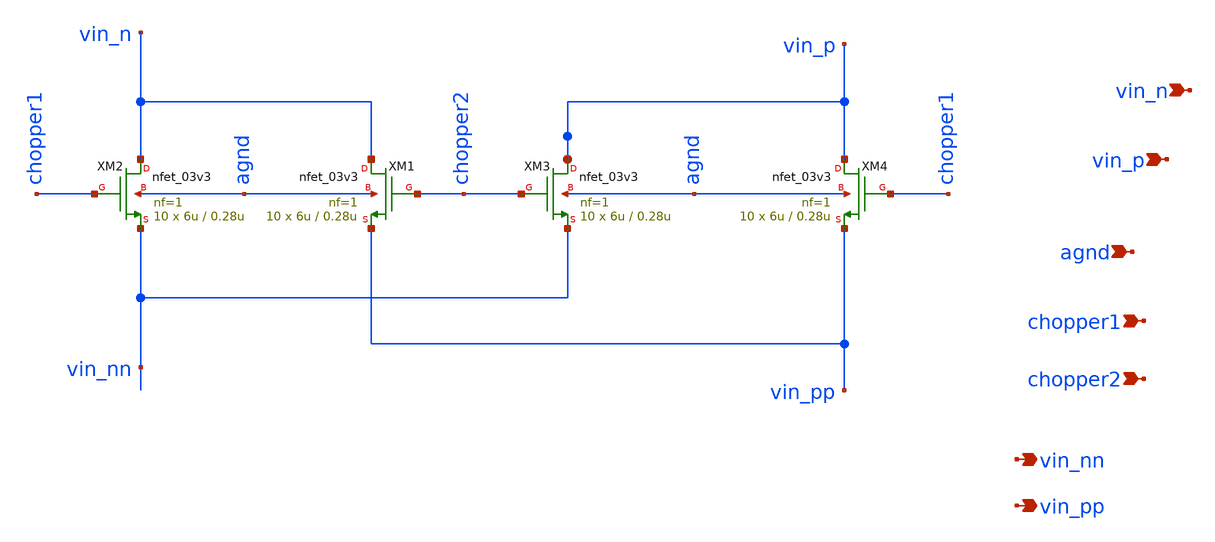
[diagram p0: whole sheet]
** sch_path: ABC123_SDC/design_data/xschem/CHOPPER/chopper.sch
**.subckt chopper vin_n vin_p agnd chopper1 chopper2 vin_nn vin_pp
*.ipin vin_n
*.ipin vin_p
*.ipin agnd
*.ipin chopper1
*.ipin chopper2
*.opin vin_nn
*.opin vin_pp
XM2 vin_n chopper1 vin_nn agnd nfet_03v3 L=0.28u W=6u nf=1 ad='int((nf+1)/2) * W/nf * 0.18u' as='int((nf+2)/2) * W/nf * 0.18u'
+ pd='2*int((nf+1)/2) * (W/nf + 0.18u)' ps='2*int((nf+2)/2) * (W/nf + 0.18u)' nrd='0.18u / W' nrs='0.18u / W'
+ sa=0 sb=0 sd=0 m=10
XM1 vin_n chopper2 vin_pp agnd nfet_03v3 L=0.28u W=6u nf=1 ad='int((nf+1)/2) * W/nf * 0.18u' as='int((nf+2)/2) * W/nf * 0.18u'
+ pd='2*int((nf+1)/2) * (W/nf + 0.18u)' ps='2*int((nf+2)/2) * (W/nf + 0.18u)' nrd='0.18u / W' nrs='0.18u / W'
+ sa=0 sb=0 sd=0 m=10
XM3 vin_p chopper2 vin_nn agnd nfet_03v3 L=0.28u W=6u nf=1 ad='int((nf+1)/2) * W/nf * 0.18u' as='int((nf+2)/2) * W/nf * 0.18u'
+ pd='2*int((nf+1)/2) * (W/nf + 0.18u)' ps='2*int((nf+2)/2) * (W/nf + 0.18u)' nrd='0.18u / W' nrs='0.18u / W'
+ sa=0 sb=0 sd=0 m=10
XM4 vin_p chopper1 vin_pp agnd nfet_03v3 L=0.28u W=6u nf=1 ad='int((nf+1)/2) * W/nf * 0.18u' as='int((nf+2)/2) * W/nf * 0.18u'
+ pd='2*int((nf+1)/2) * (W/nf + 0.18u)' ps='2*int((nf+2)/2) * (W/nf + 0.18u)' nrd='0.18u / W' nrs='0.18u / W'
+ sa=0 sb=0 sd=0 m=10
**.ends
.end
